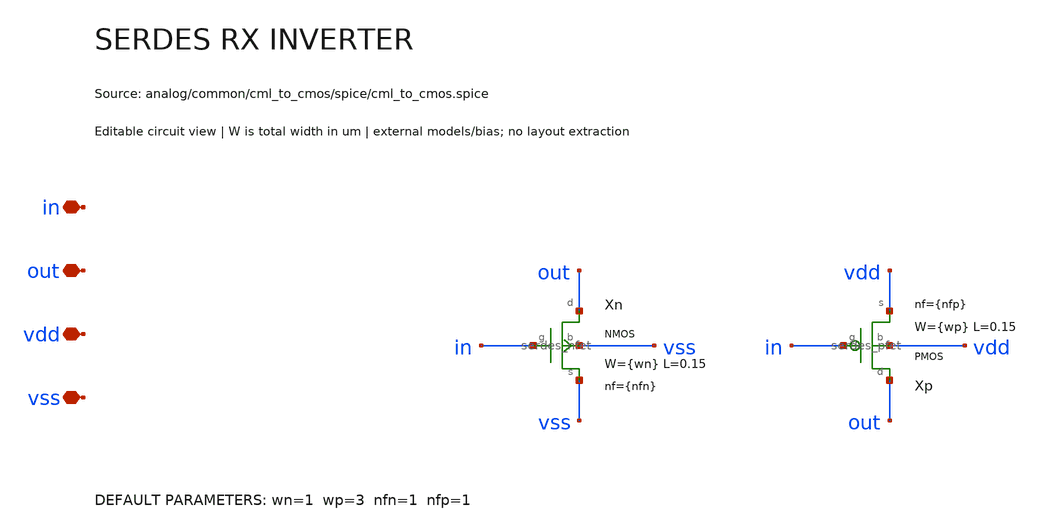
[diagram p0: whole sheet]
** sch_path: analog/common/cml_to_cmos/schematic/serdes_rx_inverter.sch
**.subckt serdes_rx_inverter in out vdd vss
*.iopin in
*.iopin out
*.iopin vdd
*.iopin vss
Xn out in vss vss serdes_nfet w={wn} l=0.15 nf={nfn}
Xp out in vdd vdd serdes_pfet w={wp} l=0.15 nf={nfp}
**.ends

* expanding   symbol:  serdes/serdes_nfet.sym # of pins=4
** sym_path: analog/common/devices/schematic/serdes_nfet.sym
** sch_path: analog/common/devices/schematic/serdes_nfet.sch
.subckt serdes_nfet d g s b  w=1 l=0.15 nf=1
*.iopin d
*.iopin g
*.iopin s
*.iopin b
Xmos d g s b sky130_fd_pr__nfet_01v8 w={w} l={l} nf={nf} ad={floor((nf+1)/2)*(w/nf)*0.29} as={floor((nf+2)/2)*(w/nf)*0.29}
+ pd={2*floor((nf+1)/2)*(w/nf+0.29)} ps={2*floor((nf+2)/2)*(w/nf+0.29)}
.ends


* expanding   symbol:  serdes/serdes_pfet.sym # of pins=4
** sym_path: analog/common/devices/schematic/serdes_pfet.sym
** sch_path: analog/common/devices/schematic/serdes_pfet.sch
.subckt serdes_pfet d g s b  w=3 l=0.15 nf=1
*.iopin d
*.iopin g
*.iopin s
*.iopin b
Xmos d g s b sky130_fd_pr__pfet_01v8 w={w} l={l} nf={nf} ad={floor((nf+1)/2)*(w/nf)*0.29} as={floor((nf+2)/2)*(w/nf)*0.29}
+ pd={2*floor((nf+1)/2)*(w/nf+0.29)} ps={2*floor((nf+2)/2)*(w/nf+0.29)}
.ends

.end
